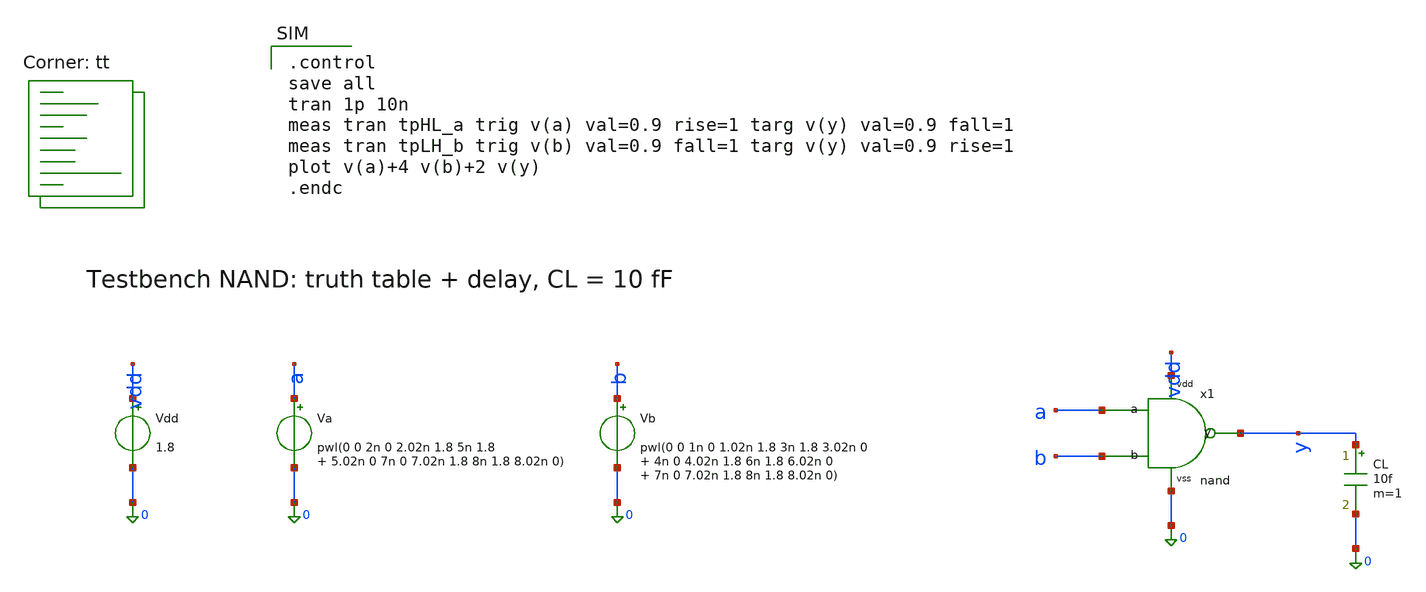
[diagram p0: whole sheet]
** sch_path: lab4/xschem/tb_nand.sch
**.subckt tb_nand
Vdd vdd 0 1.8
.save i(vdd)
Va a 0 pwl(0 0 2n 0 2.02n 1.8 5n 1.8 5.02n 0 7n 0 7.02n 1.8 8n 1.8 8.02n 0)
.save i(va)
Vb b 0 pwl(0 0 1n 0 1.02n 1.8 3n 1.8 3.02n 0 4n 0 4.02n 1.8 6n 1.8 6.02n 0 7n 0 7.02n 1.8 8n 1.8
+ 8.02n 0)
.save i(vb)
x1 a b y vdd 0 nand
CL y 0 10f m=1
**** begin user architecture code
.lib $::SKYWATER_MODELS/sky130.lib.spice tt

.control
save all
tran 1p 10n
meas tran tpHL_a trig v(a) val=0.9 rise=1 targ v(y) val=0.9 fall=1
meas tran tpLH_b trig v(b) val=0.9 fall=1 targ v(y) val=0.9 rise=1
plot v(a)+4 v(b)+2 v(y)
.endc

**** end user architecture code
**.ends

* expanding   symbol:  nand.sym # of pins=5
** sym_path: lab4/xschem/nand.sym
** sch_path: lab4/xschem/nand.sch
.subckt nand a b y vdd vss
*.ipin a
*.ipin b
*.opin y
*.iopin vdd
*.iopin vss
XMPA y a vdd vdd sky130_fd_pr__pfet_01v8 L=0.15 W=2.5 nf=1 ad='int((nf+1)/2) * W/nf * 0.29' as='int((nf+2)/2) * W/nf * 0.29'
+ pd='2*int((nf+1)/2) * (W/nf + 0.29)' ps='2*int((nf+2)/2) * (W/nf + 0.29)' nrd='0.29 / W' nrs='0.29 / W'
+ sa=0 sb=0 sd=0 mult=1 m=1
XMPB y b vdd vdd sky130_fd_pr__pfet_01v8 L=0.15 W=2.5 nf=1 ad='int((nf+1)/2) * W/nf * 0.29' as='int((nf+2)/2) * W/nf * 0.29'
+ pd='2*int((nf+1)/2) * (W/nf + 0.29)' ps='2*int((nf+2)/2) * (W/nf + 0.29)' nrd='0.29 / W' nrs='0.29 / W'
+ sa=0 sb=0 sd=0 mult=1 m=1
XMNA y a n1 vss sky130_fd_pr__nfet_01v8 L=0.15 W=2 nf=1 ad='int((1 + 1)/2) * 2 / 1 * 0.29' as='int((1 + 2)/2) * 2 / 1 * 0.29'
+ pd='2*int((1 + 1)/2) * (2 / 1 + 0.29)' ps='2*int((1 + 2)/2) * (2 / 1 + 0.29)' nrd='0.29 / 2 ' nrs='0.29 / 2 '
+ sa=0 sb=0 sd=0 mult=1 m=1
XMNB n1 b vss vss sky130_fd_pr__nfet_01v8 L=0.15 W=2 nf=1 ad='int((1 + 1)/2) * 2 / 1 * 0.29' as='int((1 + 2)/2) * 2 / 1 * 0.29'
+ pd='2*int((1 + 1)/2) * (2 / 1 + 0.29)' ps='2*int((1 + 2)/2) * (2 / 1 + 0.29)' nrd='0.29 / 2 ' nrs='0.29 / 2 '
+ sa=0 sb=0 sd=0 mult=1 m=1
.ends

.end
